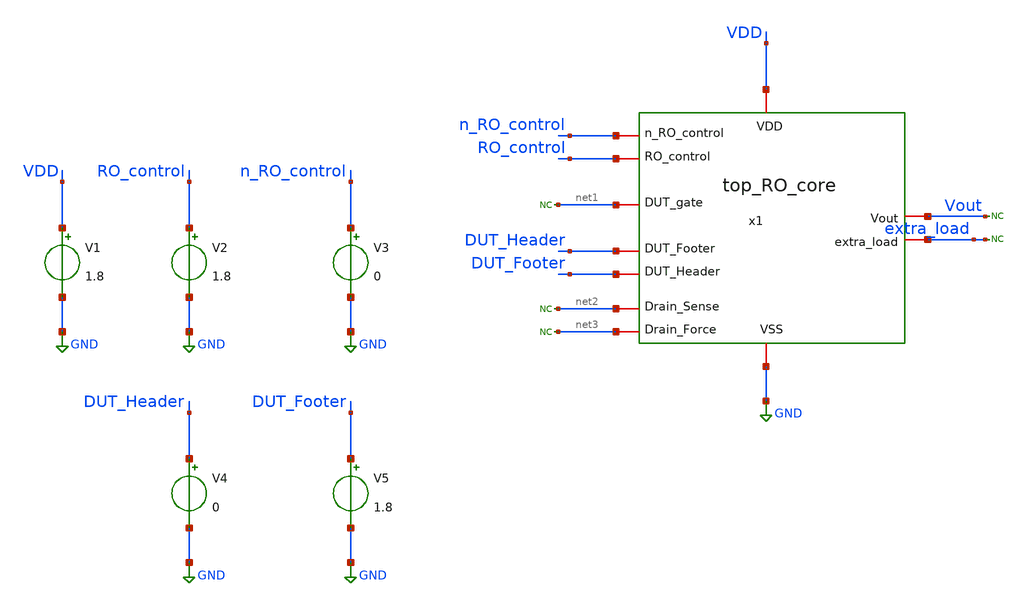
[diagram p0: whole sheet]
** sch_path: TT/top_RO_core_tb.sch
.lib $::SKYWATER_MODELS/sky130.lib.spice tt
.include $::SKYWATER_STDCELLS/sky130_fd_sc_hd.spice

**.subckt top_RO_core_tb
x1 VDD GND n_RO_control RO_control net1 Vout DUT_Footer DUT_Header net3 net2 extra_load top_RO_core
V1 VDD GND 1.8
V2 RO_control GND 1.8
V3 n_RO_control GND 0
* noconn #net1
V4 DUT_Header GND 0
V5 DUT_Footer GND 1.8
* noconn #net2
* noconn #net3
* noconn extra_load
* noconn Vout
**** begin user architecture code


.ic V(out)=0.8
.tran 0.1n 50n
.save all



**** end user architecture code
**.ends
.GLOBAL GND
.end
